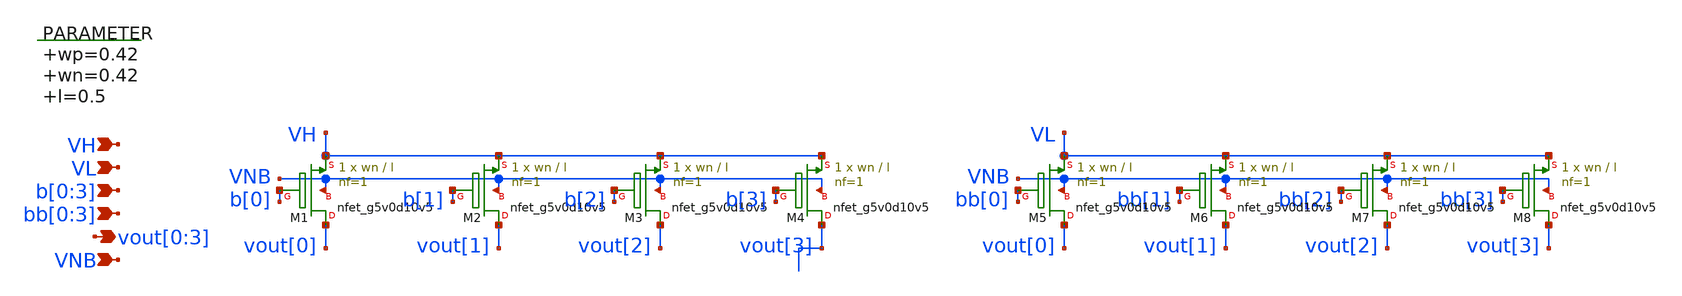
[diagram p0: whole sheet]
** sch_path: xschem/interpolating_dec_4b.sch
**.subckt interpolating_dec_4b vout[0],vout[1],vout[2],vout[3] VNB b[0],b[1],b[2],b[3] VH VL
*+ bb[0],bb[1],bb[2],bb[3]
*.opin vout[0],vout[1],vout[2],vout[3]
*.ipin VNB
*.ipin b[0],b[1],b[2],b[3]
*.ipin VH
*.ipin VL
*.ipin bb[0],bb[1],bb[2],bb[3]
.param wp=0.42 wn=0.42 l=0.5

XM1 vout[0] b[0] VH VNB sky130_fd_pr__nfet_g5v0d10v5 L=l W=wn nf=1 ad='int((nf+1)/2) * W/nf * 0.29' as='int((nf+2)/2) * W/nf * 0.29'
+ pd='2*int((nf+1)/2) * (W/nf + 0.29)' ps='2*int((nf+2)/2) * (W/nf + 0.29)' nrd='0.29 / W' nrs='0.29 / W'
+ sa=0 sb=0 sd=0 mult=1 m=1
XM2 vout[1] b[1] VH VNB sky130_fd_pr__nfet_g5v0d10v5 L=l W=wn nf=1 ad='int((nf+1)/2) * W/nf * 0.29' as='int((nf+2)/2) * W/nf * 0.29'
+ pd='2*int((nf+1)/2) * (W/nf + 0.29)' ps='2*int((nf+2)/2) * (W/nf + 0.29)' nrd='0.29 / W' nrs='0.29 / W'
+ sa=0 sb=0 sd=0 mult=1 m=1
XM3 vout[2] b[2] VH VNB sky130_fd_pr__nfet_g5v0d10v5 L=l W=wn nf=1 ad='int((nf+1)/2) * W/nf * 0.29' as='int((nf+2)/2) * W/nf * 0.29'
+ pd='2*int((nf+1)/2) * (W/nf + 0.29)' ps='2*int((nf+2)/2) * (W/nf + 0.29)' nrd='0.29 / W' nrs='0.29 / W'
+ sa=0 sb=0 sd=0 mult=1 m=1
XM4 vout[3] b[3] VH VNB sky130_fd_pr__nfet_g5v0d10v5 L=l W=wn nf=1 ad='int((nf+1)/2) * W/nf * 0.29' as='int((nf+2)/2) * W/nf * 0.29'
+ pd='2*int((nf+1)/2) * (W/nf + 0.29)' ps='2*int((nf+2)/2) * (W/nf + 0.29)' nrd='0.29 / W' nrs='0.29 / W'
+ sa=0 sb=0 sd=0 mult=1 m=1
XM5 vout[0] bb[0] VL VNB sky130_fd_pr__nfet_g5v0d10v5 L=l W=wn nf=1 ad='int((nf+1)/2) * W/nf * 0.29'
+ as='int((nf+2)/2) * W/nf * 0.29' pd='2*int((nf+1)/2) * (W/nf + 0.29)' ps='2*int((nf+2)/2) * (W/nf + 0.29)'
+ nrd='0.29 / W' nrs='0.29 / W' sa=0 sb=0 sd=0 mult=1 m=1
XM6 vout[1] bb[1] VL VNB sky130_fd_pr__nfet_g5v0d10v5 L=l W=wn nf=1 ad='int((nf+1)/2) * W/nf * 0.29'
+ as='int((nf+2)/2) * W/nf * 0.29' pd='2*int((nf+1)/2) * (W/nf + 0.29)' ps='2*int((nf+2)/2) * (W/nf + 0.29)'
+ nrd='0.29 / W' nrs='0.29 / W' sa=0 sb=0 sd=0 mult=1 m=1
XM7 vout[2] bb[2] VL VNB sky130_fd_pr__nfet_g5v0d10v5 L=l W=wn nf=1 ad='int((nf+1)/2) * W/nf * 0.29'
+ as='int((nf+2)/2) * W/nf * 0.29' pd='2*int((nf+1)/2) * (W/nf + 0.29)' ps='2*int((nf+2)/2) * (W/nf + 0.29)'
+ nrd='0.29 / W' nrs='0.29 / W' sa=0 sb=0 sd=0 mult=1 m=1
XM8 vout[3] bb[3] VL VNB sky130_fd_pr__nfet_g5v0d10v5 L=l W=wn nf=1 ad='int((nf+1)/2) * W/nf * 0.29'
+ as='int((nf+2)/2) * W/nf * 0.29' pd='2*int((nf+1)/2) * (W/nf + 0.29)' ps='2*int((nf+2)/2) * (W/nf + 0.29)'
+ nrd='0.29 / W' nrs='0.29 / W' sa=0 sb=0 sd=0 mult=1 m=1
**.ends
.end
